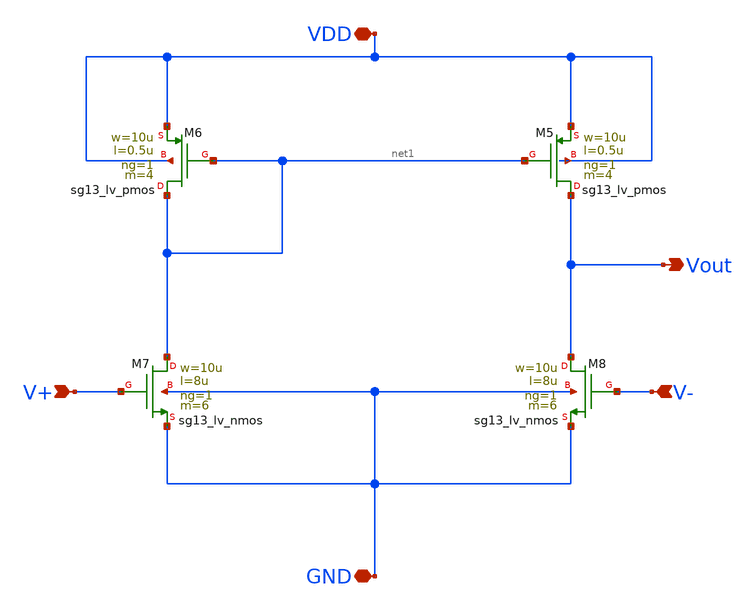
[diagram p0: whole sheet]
** sch_path: SSDOR_1.2V_v2/components/Ib_4u/Ib_4u_opamp/Ib_4u_opamp.sch
**.subckt Ib_4u_opamp VDD V+ V- GND Vout
*.iopin VDD
*.ipin V+
*.ipin V-
*.iopin GND
*.opin Vout
XM5 Vout net1 VDD VDD sg13_lv_pmos w=10u l=0.5u ng=1 m=4 mm_ok=1
XM6 net1 net1 VDD VDD sg13_lv_pmos w=10u l=0.5u ng=1 m=4 mm_ok=1
XM7 net1 V+ GND GND sg13_lv_nmos w=10u l=8u ng=1 m=6 mm_ok=1
XM8 Vout V- GND GND sg13_lv_nmos w=10u l=8u ng=1 m=6 mm_ok=1
**.ends
.end
